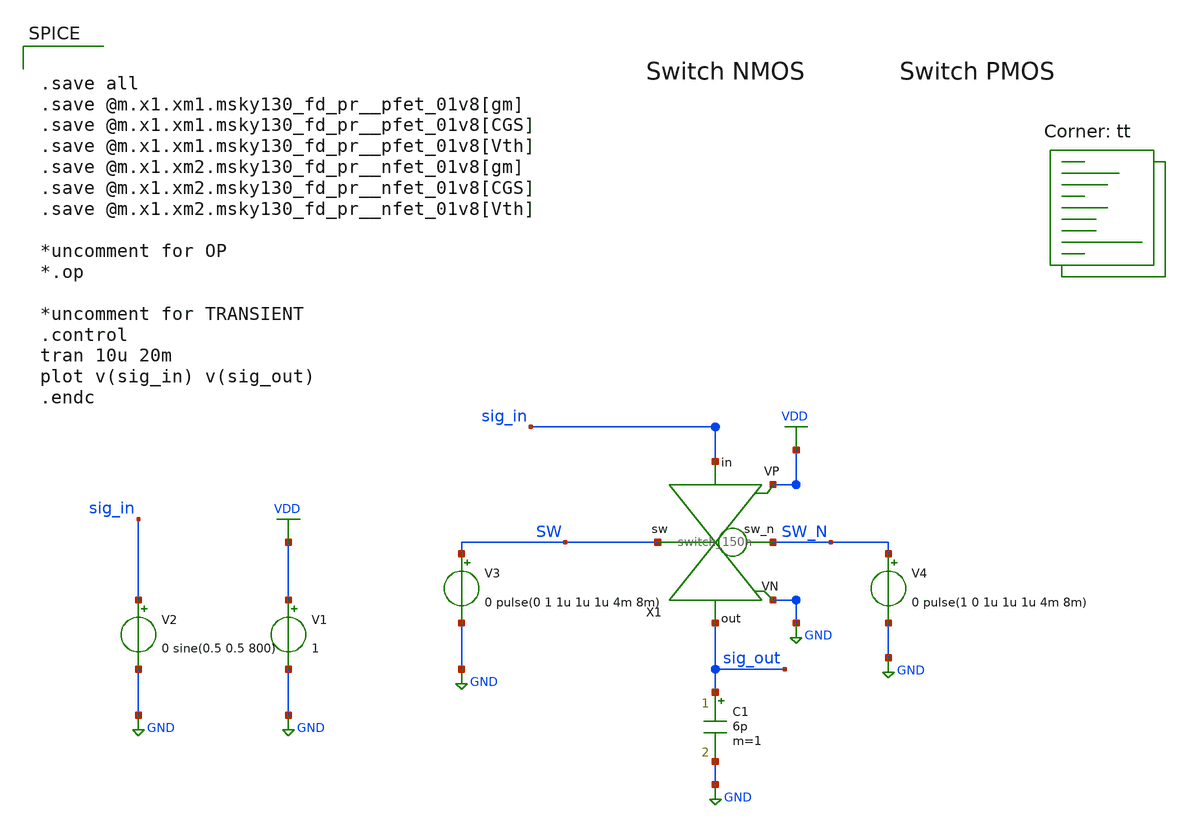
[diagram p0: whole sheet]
** sch_path: xschem/switch_150n/switch_150n_tb.sch
* xschem/switch/switch_150n.sch:
* Copyright 2022 Manuel Moser
* Licensed under the Apache License, Version 2.0 (the "License");
**.subckt switch_150n_tb
V1 VDD GND 1
V2 sig_in GND 0 sine(0.5 0.5 800)
V3 SW GND 0 pulse(0 1 1u 1u 1u 4m 8m)
V4 SW_N GND 0 pulse(1 0 1u 1u 1u 4m 8m)
X1 SW_N sig_in SW sig_out VDD GND switch_150n
C1 sig_out GND 6p m=1
**** begin user architecture code


.save all
.save @m.x1.xm1.msky130_fd_pr__pfet_01v8[gm]
.save @m.x1.xm1.msky130_fd_pr__pfet_01v8[CGS]
.save @m.x1.xm1.msky130_fd_pr__pfet_01v8[Vth]
.save @m.x1.xm2.msky130_fd_pr__nfet_01v8[gm]
.save @m.x1.xm2.msky130_fd_pr__nfet_01v8[CGS]
.save @m.x1.xm2.msky130_fd_pr__nfet_01v8[Vth]

*uncomment for OP
*.op

*uncomment for TRANSIENT
.control
tran 10u 20m
plot v(sig_in) v(sig_out)
.endc


.lib $::SKYWATER_MODELS/sky130.lib.spice tt
**** end user architecture code
**.ends

* expanding   symbol:  switch_150n.sym # of pins=6
** sym_path: xschem/switch/switch_150n.sym
** sch_path: xschem/switch/switch_150n.sch
.subckt switch_150n sw_n in sw out VP VN
*.iopin VN
*.iopin VP
*.ipin IN
*.opin OUT
*.ipin SW_N
*.ipin SW
XM2 IN SW OUT VN sky130_fd_pr__nfet_01v8_lvt L=0.35 W=2 nf=1 ad='int((nf+1)/2) * W/nf * 0.29' as='int((nf+2)/2) * W/nf * 0.29'
+ pd='2*int((nf+1)/2) * (W/nf + 0.29)' ps='2*int((nf+2)/2) * (W/nf + 0.29)' nrd='0.29 / W' nrs='0.29 / W'
+ sa=0 sb=0 sd=0 mult=1 m=1
XM1 IN SW_N OUT VP sky130_fd_pr__pfet_01v8 L=0.15 W=1.7 nf=1 ad='int((nf+1)/2) * W/nf * 0.29' as='int((nf+2)/2) * W/nf * 0.29'
+ pd='2*int((nf+1)/2) * (W/nf + 0.29)' ps='2*int((nf+2)/2) * (W/nf + 0.29)' nrd='0.29 / W' nrs='0.29 / W'
+ sa=0 sb=0 sd=0 mult=1 m=1
.ends

.GLOBAL GND
.GLOBAL VDD
.end
